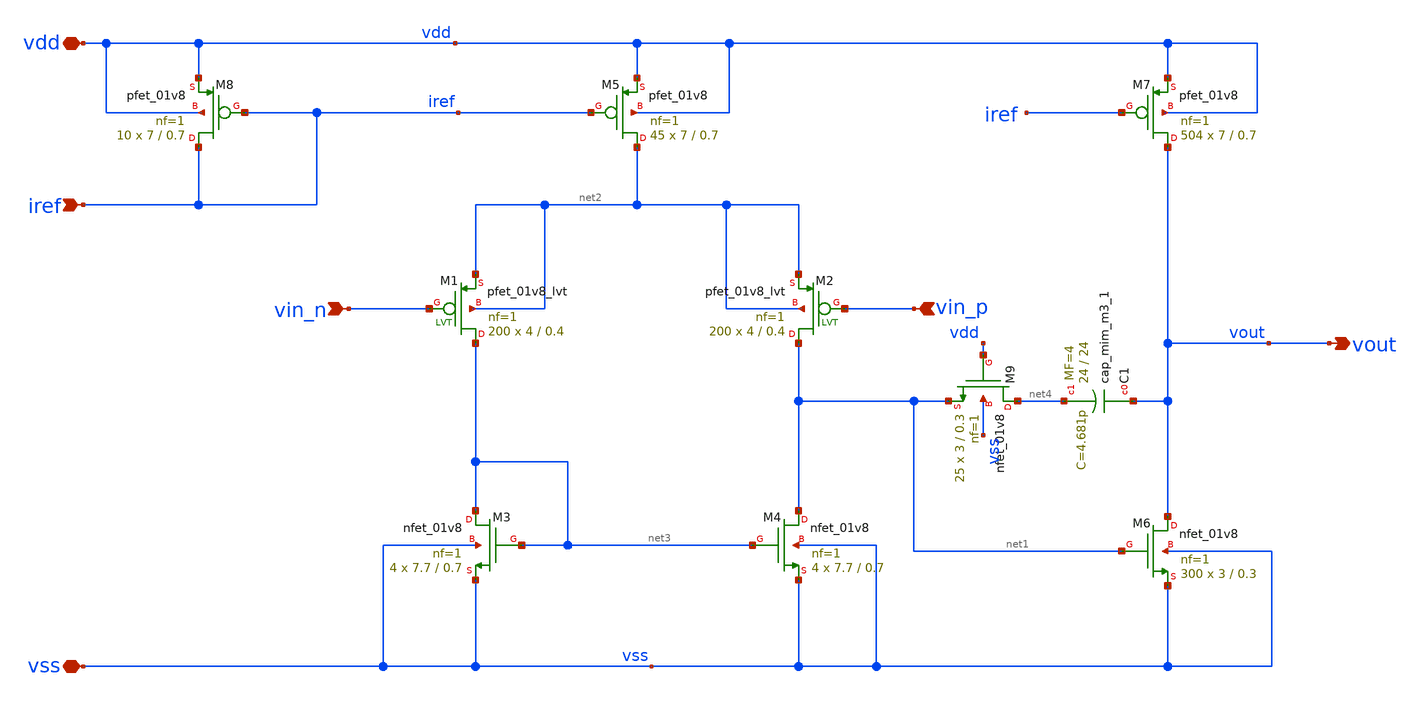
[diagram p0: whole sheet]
** sch_path: xschem/opamp_lucas.sch
**.subckt opamp_lucas vdd vss vin_n vin_p iref vout
*.iopin vdd
*.iopin vss
*.ipin vin_n
*.ipin vin_p
*.ipin iref
*.opin vout
XM3 net3 net3 vss vss sky130_fd_pr__nfet_01v8 L=0.7 W=7.7 nf=1 ad='W * 0.29' as='W * 0.29' pd='2 * (W + 0.29)'
+ ps='2 * (W + 0.29)' nrd='0.29 / W' nrs='0.29 / W' sa=0 sb=0 sd=0 mult=4 m=4
XM5 net2 iref vdd vdd sky130_fd_pr__pfet_01v8 L=0.7 W=7 nf=1 ad='W * 0.29' as='W * 0.29' pd='2 * (W + 0.29)'
+ ps='2 * (W + 0.29)' nrd='0.29 / W' nrs='0.29 / W' sa=0 sb=0 sd=0 mult=45 m=45
XM7 vout iref vdd vdd sky130_fd_pr__pfet_01v8 L=0.7 W=7 nf=1 ad='W * 0.29' as='W * 0.29' pd='2 * (W + 0.29)'
+ ps='2 * (W + 0.29)' nrd='0.29 / W' nrs='0.29 / W' sa=0 sb=0 sd=0 mult=504 m=504
XM8 iref iref vdd vdd sky130_fd_pr__pfet_01v8 L=0.7 W=7 nf=1 ad='W * 0.29' as='W * 0.29' pd='2 * (W + 0.29)'
+ ps='2 * (W + 0.29)' nrd='0.29 / W' nrs='0.29 / W' sa=0 sb=0 sd=0 mult=10 m=10
XM6 vout net1 vss vss sky130_fd_pr__nfet_01v8 L=0.3 W=3 nf=1 ad='W * 0.29' as='W * 0.29' pd='2 * (W + 0.29)'
+ ps='2 * (W + 0.29)' nrd='0.29 / W' nrs='0.29 / W' sa=0 sb=0 sd=0 mult=300 m=300
XM1 net3 vin_n net2 net2 sky130_fd_pr__pfet_01v8_lvt L=0.4 W=4 nf=1 ad='int((nf+1)/2) * W/nf * 0.29'
+ as='int((nf+2)/2) * W/nf * 0.29' pd='2*int((nf+1)/2) * (W/nf + 0.29)' ps='2*int((nf+2)/2) * (W/nf + 0.29)'
+ nrd='0.29 / W' nrs='0.29 / W' sa=0 sb=0 sd=0 mult=200 m=200
XM2 net1 vin_p net2 net2 sky130_fd_pr__pfet_01v8_lvt L=0.4 W=4 nf=1 ad='int((nf+1)/2) * W/nf * 0.29'
+ as='int((nf+2)/2) * W/nf * 0.29' pd='2*int((nf+1)/2) * (W/nf + 0.29)' ps='2*int((nf+2)/2) * (W/nf + 0.29)'
+ nrd='0.29 / W' nrs='0.29 / W' sa=0 sb=0 sd=0 mult=200 m=200
XM9 net4 vdd net1 vss sky130_fd_pr__nfet_01v8 L=0.3 W=3 nf=1 ad='int((nf+1)/2) * W/nf * 0.29' as='int((nf+2)/2) * W/nf * 0.29'
+ pd='2*int((nf+1)/2) * (W/nf + 0.29)' ps='2*int((nf+2)/2) * (W/nf + 0.29)' nrd='0.29 / W' nrs='0.29 / W'
+ sa=0 sb=0 sd=0 mult=25 m=25
XC1 vout net4 sky130_fd_pr__cap_mim_m3_1 W=24 L=24 MF=4 m=4
XM4 net1 net3 vss vss sky130_fd_pr__nfet_01v8 L=0.7 W=7.7 nf=1 ad='W * 0.29' as='W * 0.29' pd='2 * (W + 0.29)'
+ ps='2 * (W + 0.29)' nrd='0.29 / W' nrs='0.29 / W' sa=0 sb=0 sd=0 mult=4 m=4
**.ends
.end
